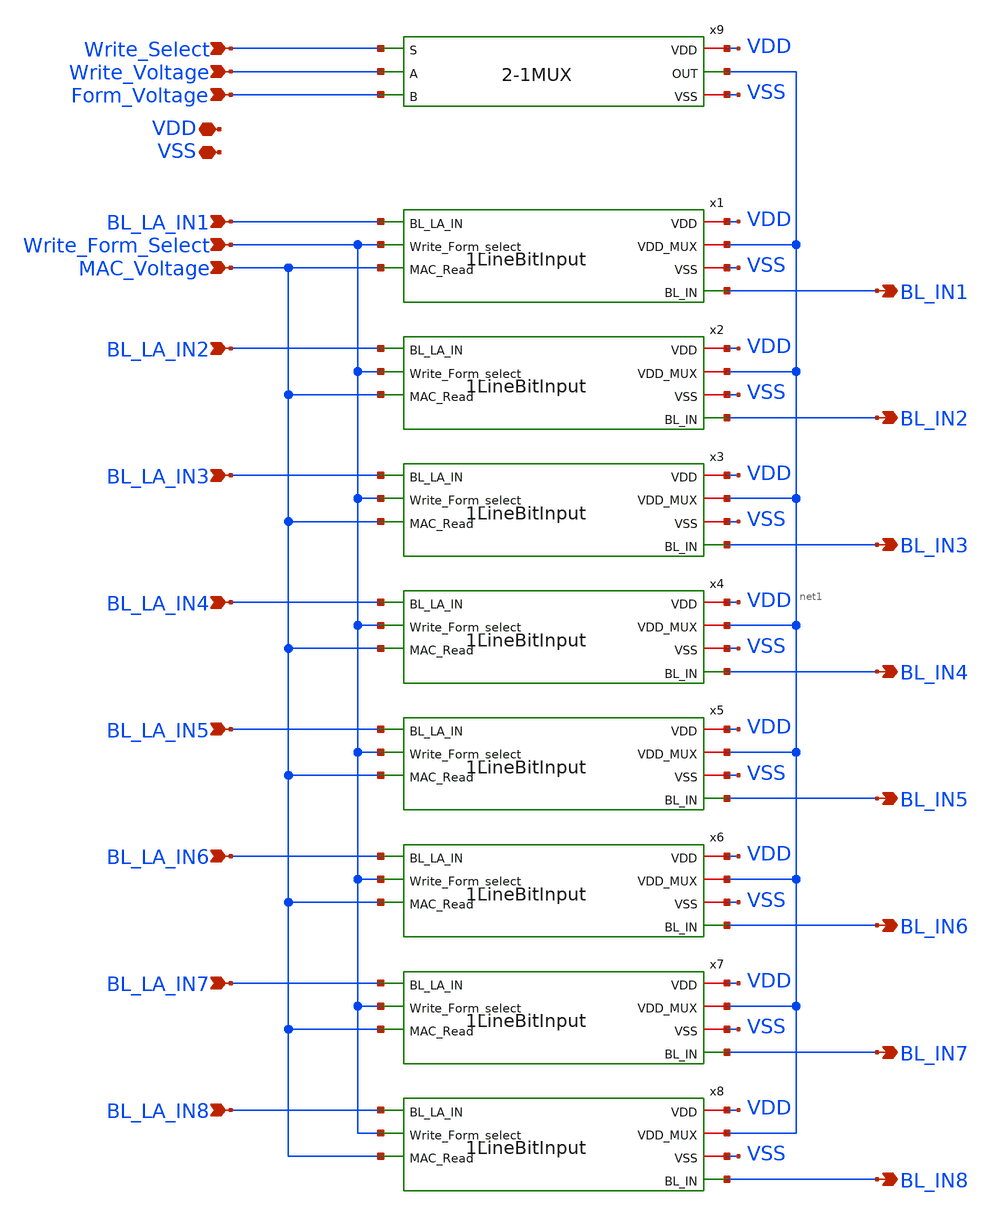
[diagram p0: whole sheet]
** sch_path: xschem/8LineBitInput.sch
**.subckt 8LineBitInput Write_Select Write_Voltage Form_Voltage BL_LA_IN1 BL_LA_IN3 BL_LA_IN6
*+ BL_LA_IN4 BL_LA_IN5 BL_LA_IN7 BL_LA_IN8 BL_LA_IN2 Write_Form_Select MAC_Voltage BL_IN1 BL_IN2 BL_IN3 BL_IN4
*+ BL_IN5 BL_IN6 BL_IN7 BL_IN8 VDD VSS
*.ipin Write_Select
*.ipin Write_Voltage
*.ipin Form_Voltage
*.ipin BL_LA_IN1
*.ipin BL_LA_IN3
*.ipin BL_LA_IN6
*.ipin BL_LA_IN4
*.ipin BL_LA_IN5
*.ipin BL_LA_IN7
*.ipin BL_LA_IN8
*.ipin BL_LA_IN2
*.ipin Write_Form_Select
*.ipin MAC_Voltage
*.opin BL_IN1
*.opin BL_IN2
*.opin BL_IN3
*.opin BL_IN4
*.opin BL_IN5
*.opin BL_IN6
*.opin BL_IN7
*.opin BL_IN8
*.iopin VDD
*.iopin VSS
x1 VDD net1 VSS BL_LA_IN1 Write_Form_Select BL_IN1 MAC_Voltage 1LineBitInput
x2 VDD net1 VSS BL_LA_IN2 Write_Form_Select BL_IN2 MAC_Voltage 1LineBitInput
x3 VDD net1 VSS BL_LA_IN3 Write_Form_Select BL_IN3 MAC_Voltage 1LineBitInput
x4 VDD net1 VSS BL_LA_IN4 Write_Form_Select BL_IN4 MAC_Voltage 1LineBitInput
x5 VDD net1 VSS BL_LA_IN5 Write_Form_Select BL_IN5 MAC_Voltage 1LineBitInput
x6 VDD net1 VSS BL_LA_IN6 Write_Form_Select BL_IN6 MAC_Voltage 1LineBitInput
x7 VDD net1 VSS BL_LA_IN7 Write_Form_Select BL_IN7 MAC_Voltage 1LineBitInput
x8 VDD net1 VSS BL_LA_IN8 Write_Form_Select BL_IN8 MAC_Voltage 1LineBitInput
x9 VDD Write_Select Write_Voltage net1 Form_Voltage VSS 2-1MUX
**.ends

* expanding   symbol:  1LineBitInput.sym # of pins=7
** sym_path: xschem/1LineBitInput.sym
** sch_path: xschem/1LineBitInput.sch
.subckt 1LineBitInput VDD VDD_MUX VSS BL_LA_IN Write_Form_select BL_IN MAC_Read
*.ipin BL_LA_IN
*.ipin Write_Form_select
*.ipin MAC_Read
*.iopin VDD
*.iopin VDD_MUX
*.iopin VSS
*.opin BL_IN
x2 VDD Write_Form_select net1 BL_IN MAC_Read VSS 2-1MUX
x3 VDD_MUX BL_LA_IN net1 VSS Buffer
.ends


* expanding   symbol:  2-1MUX.sym # of pins=6
** sym_path: xschem/2-1MUX.sym
** sch_path: xschem/2-1MUX.sch
.subckt 2-1MUX VDD S A OUT B VSS
*.ipin A
*.ipin B
*.ipin S
*.iopin VDD
*.iopin VSS
*.opin OUT
x1 net1 VDD OUT A VSS S TransmissionGate
x2 S VDD OUT B VSS net1 TransmissionGate
x3 VDD S net1 VSS Inverter
.ends


* expanding   symbol:  Buffer.sym # of pins=4
** sym_path: xschem/Buffer.sym
** sch_path: xschem/Buffer.sch
.subckt Buffer VDD Vin Vout VSS
*.iopin VDD
*.iopin VSS
*.ipin Vin
*.opin Vout
x1 VDD Vin net1 VSS Inverter
x2 VDD net1 Vout VSS Inverter
.ends


* expanding   symbol:  TransmissionGate.sym # of pins=6
** sym_path: xschem/TransmissionGate.sym
** sch_path: xschem/TransmissionGate.sch
.subckt TransmissionGate SP VDD Out In VSS SN
*.opin Out
*.ipin In
*.ipin SP
*.iopin VDD
*.iopin VSS
*.ipin SN
XM1 In SN Out VSS sky130_fd_pr__nfet_g5v0d10v5 L=0.5 W=0.75 nf=1 ad='int((nf+1)/2) * W/nf * 0.29' as='int((nf+2)/2) * W/nf * 0.29'
+ pd='2*int((nf+1)/2) * (W/nf + 0.29)' ps='2*int((nf+2)/2) * (W/nf + 0.29)' nrd='0.29 / W' nrs='0.29 / W'
+ sa=0 sb=0 sd=0 mult=1 m=1
XM2 In SP Out VDD sky130_fd_pr__pfet_g5v0d10v5 L=0.5 W=1.5 nf=1 ad='int((nf+1)/2) * W/nf * 0.29' as='int((nf+2)/2) * W/nf * 0.29'
+ pd='2*int((nf+1)/2) * (W/nf + 0.29)' ps='2*int((nf+2)/2) * (W/nf + 0.29)' nrd='0.29 / W' nrs='0.29 / W'
+ sa=0 sb=0 sd=0 mult=1 m=1
.ends


* expanding   symbol:  Inverter.sym # of pins=4
** sym_path: xschem/Inverter.sym
** sch_path: xschem/Inverter.sch
.subckt Inverter VDD Vin Vout VSS
*.ipin Vin
*.iopin VDD
*.iopin VSS
*.opin Vout
XM1 Vout Vin VSS VSS sky130_fd_pr__nfet_g5v0d10v5 L=0.5 W=0.75 nf=1 ad='int((nf+1)/2) * W/nf * 0.29'
+ as='int((nf+2)/2) * W/nf * 0.29' pd='2*int((nf+1)/2) * (W/nf + 0.29)' ps='2*int((nf+2)/2) * (W/nf + 0.29)'
+ nrd='0.29 / W' nrs='0.29 / W' sa=0 sb=0 sd=0 mult=1 m=1
XM2 Vout Vin VDD VDD sky130_fd_pr__pfet_g5v0d10v5 L=0.5 W=1.5 nf=1 ad='int((nf+1)/2) * W/nf * 0.29' as='int((nf+2)/2) * W/nf * 0.29'
+ pd='2*int((nf+1)/2) * (W/nf + 0.29)' ps='2*int((nf+2)/2) * (W/nf + 0.29)' nrd='0.29 / W' nrs='0.29 / W'
+ sa=0 sb=0 sd=0 mult=1 m=1
.ends

.end
